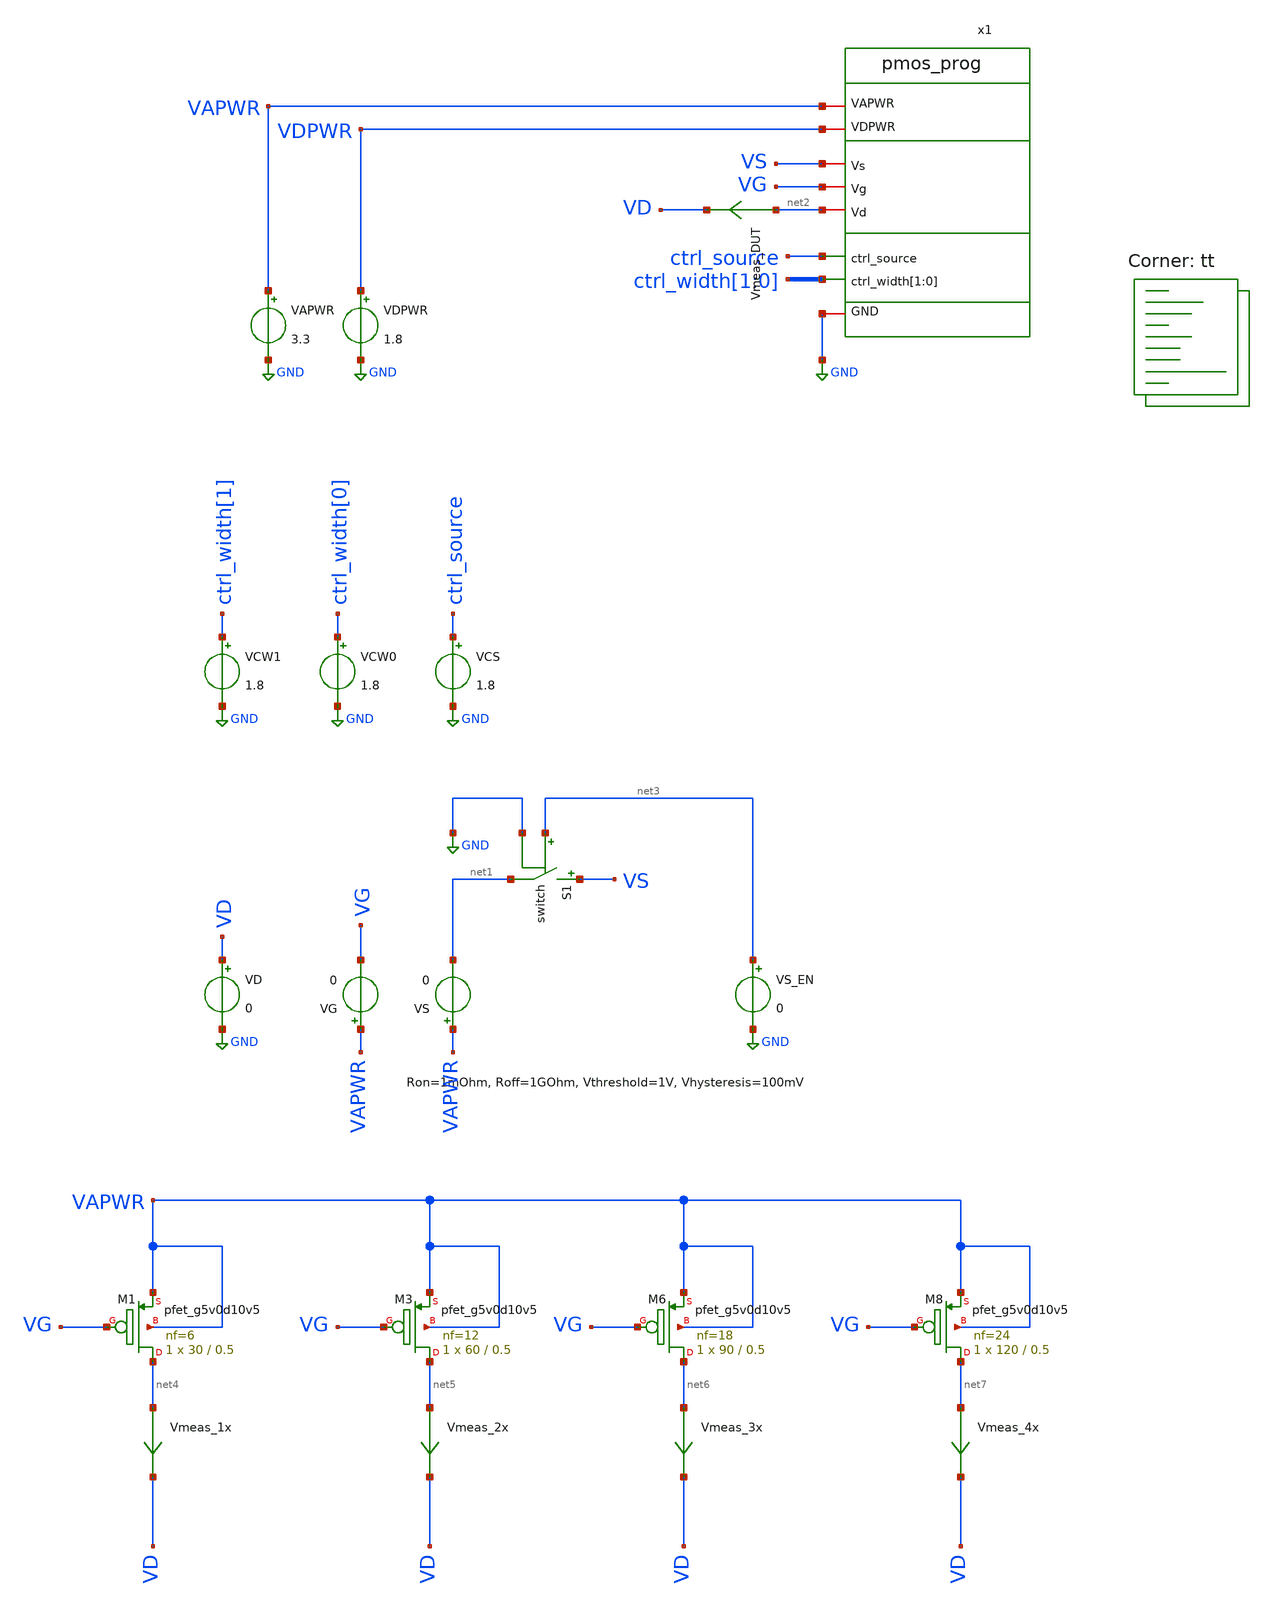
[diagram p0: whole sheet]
** sch_path: xschem/tb_pmos_prog.sch
**.subckt tb_pmos_prog
VAPWR VAPWR GND 3.3
VDPWR VDPWR GND 1.8
VCW1 ctrl_width[1] GND 1.8
VCW0 ctrl_width[0] GND 1.8
VCS ctrl_source GND 1.8
VD VD GND 0
VG VAPWR VG 0
VS VAPWR net1 0
VS_EN net3 GND 0
S1 VS net1 net3 GND switch
Vmeas_1x net4 VD 0
.save i(vmeas_1x)
Vmeas_DUT net2 VD 0
.save i(vmeas_dut)
Vmeas_2x net5 VD 0
.save i(vmeas_2x)
Vmeas_4x net7 VD 0
.save i(vmeas_4x)
Vmeas_3x net6 VD 0
.save i(vmeas_3x)
x1 VAPWR VDPWR VS VG net2 ctrl_source ctrl_width[1] ctrl_width[0] GND pmos_prog
XM1 net4 VG VAPWR VAPWR sky130_fd_pr__pfet_g5v0d10v5 L=0.5 W=30 nf=6 ad='int((nf+1)/2) * W/nf * 0.29'
+ as='int((nf+2)/2) * W/nf * 0.29' pd='2*int((nf+1)/2) * (W/nf + 0.29)' ps='2*int((nf+2)/2) * (W/nf + 0.29)'
+ nrd='0.29 / W' nrs='0.29 / W' sa=0 sb=0 sd=0 mult=1 m=1
XM3 net5 VG VAPWR VAPWR sky130_fd_pr__pfet_g5v0d10v5 L=0.5 W=60 nf=12 ad='int((nf+1)/2) * W/nf * 0.29'
+ as='int((nf+2)/2) * W/nf * 0.29' pd='2*int((nf+1)/2) * (W/nf + 0.29)' ps='2*int((nf+2)/2) * (W/nf + 0.29)'
+ nrd='0.29 / W' nrs='0.29 / W' sa=0 sb=0 sd=0 mult=1 m=1
XM6 net6 VG VAPWR VAPWR sky130_fd_pr__pfet_g5v0d10v5 L=0.5 W=90 nf=18 ad='int((nf+1)/2) * W/nf * 0.29'
+ as='int((nf+2)/2) * W/nf * 0.29' pd='2*int((nf+1)/2) * (W/nf + 0.29)' ps='2*int((nf+2)/2) * (W/nf + 0.29)'
+ nrd='0.29 / W' nrs='0.29 / W' sa=0 sb=0 sd=0 mult=1 m=1
XM8 net7 VG VAPWR VAPWR sky130_fd_pr__pfet_g5v0d10v5 L=0.5 W=120 nf=24 ad='int((nf+1)/2) * W/nf * 0.29'
+ as='int((nf+2)/2) * W/nf * 0.29' pd='2*int((nf+1)/2) * (W/nf + 0.29)' ps='2*int((nf+2)/2) * (W/nf + 0.29)'
+ nrd='0.29 / W' nrs='0.29 / W' sa=0 sb=0 sd=0 mult=1 m=1
**** begin user architecture code
.lib $::SKYWATER_MODELS/sky130.lib.spice tt


*****************************************
* VGS Sweep Test
*****************************************
* this test does a ID vs VGS DC sweep for a common source configuration
* and plots the current vs ideal PMOS devices.
* plots 1-4 represent each programmed PMOS width
*****************************************
.model switch SW(Ron=1m, Roff=1G, Vt=0.5, Vh=0.1)
.control
   save all
   set temp = 27
   set wr_singlescale
   set wr_vecnames
   alter VD 0
   alter VCW1 0
   alter VCW0 0
   alter VCS 1.8
   alter VS_EN 0
   repeat 2
      repeat 2
         dc VG 0 3.3 0.01
         alter VCW0 1.8
      end
      alter VCW1 1.8
      alter VCW0 0
   end
   plot dc1.i(Vmeas_DUT) dc1.i(Vmeas_1x); ylog
   plot dc4.i(Vmeas_DUT) dc4.i(Vmeas_4x); ylog
   plot deriv(dc1.i(Vmeas_DUT)) deriv(dc1.i(Vmeas_1x))
   plot deriv(dc4.i(Vmeas_DUT)) deriv(dc4.i(Vmeas_4x))
.endc


**** end user architecture code
**.ends
.GLOBAL GND
.end
